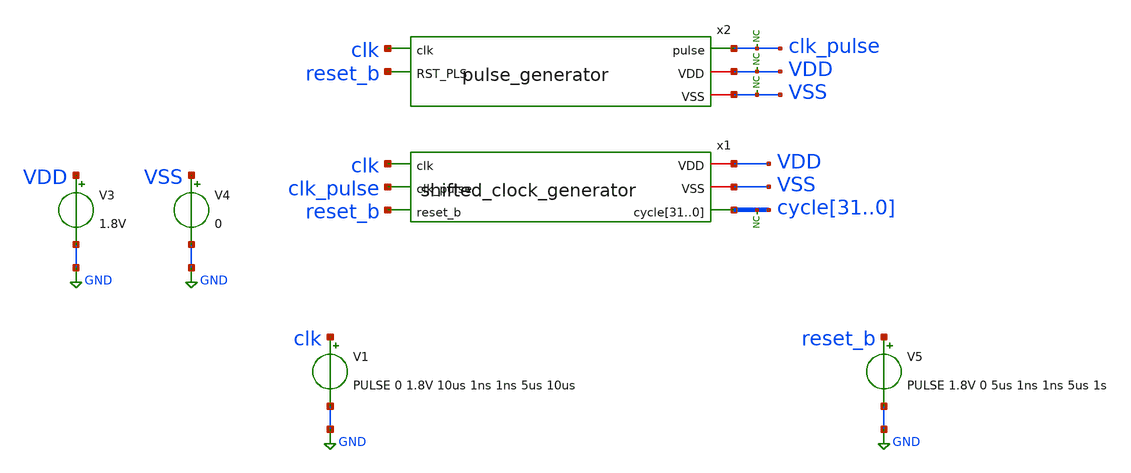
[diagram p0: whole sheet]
** sch_path: xschem/tests/shifted_clock_generator/pulse_generator_and_shifted_clock_generator_test.sch
**.subckt pulse_generator_and_shifted_clock_generator_test
V3 VDD GND 1.8V
V4 VSS GND 0
* noconn cycle[31..0]
V1 clk GND PULSE 0 1.8V 10us 1ns 1ns 5us 10us
V5 reset_b GND PULSE 1.8V 0 5us 1ns 1ns 5us 1s
* noconn clk_pulse
* noconn VDD
* noconn VSS
x2 clk clk_pulse VDD VSS reset_b pulse_generator
x1 clk VDD VSS clk_pulse reset_b cycle31 cycle30 cycle29 cycle28 cycle27 cycle26 cycle25 cycle24
+ cycle23 cycle22 cycle21 cycle20 cycle19 cycle18 cycle17 cycle16 cycle15 cycle14 cycle13 cycle12 cycle11
+ cycle10 cycle9 cycle8 cycle7 cycle6 cycle5 cycle4 cycle3 cycle2 cycle1 cycle0 shifted_clock_generator
**** begin user architecture code
 .lib $::SKYWATER_MODELS/sky130.lib.spice tt
.include $::SKYWATER_STDCELLS/sky130_fd_sc_hd.spice


.options acct list
.temp 25
*vvcc VDD 0 dc 1.8
*vvss VSS 0 0
.control
save all
tran 0.1u 350u
*plot RST_PLS clk+2 Pulse+4
plot reset_b-6 clk-4 clk_pulse-2 cycle0 cycle1+2 cycle2+4 cycle3+6 cycle4+8 cycle5+10 cycle6+12
+ cycle7+14 cycle8+16 cycle9+18 cycle10+20 cycle11+22 cycle12+24 cycle13+26 cycle14+28 cycle15+30 cycle16+32
+ cycle17+34 cycle18+36 cycle19+38 cycle20+40 cycle21+42 cycle22+44  cycle23+46 cycle24+48 cycle25+50 cycle26+52
+ cycle27+54 cycle28+56 cycle29+58 cycle30+60 cycle31+62

write pulse_generator_and_shifted_clock_generator_test.raw
.endc


**** end user architecture code
**.ends
.GLOBAL GND
.end
